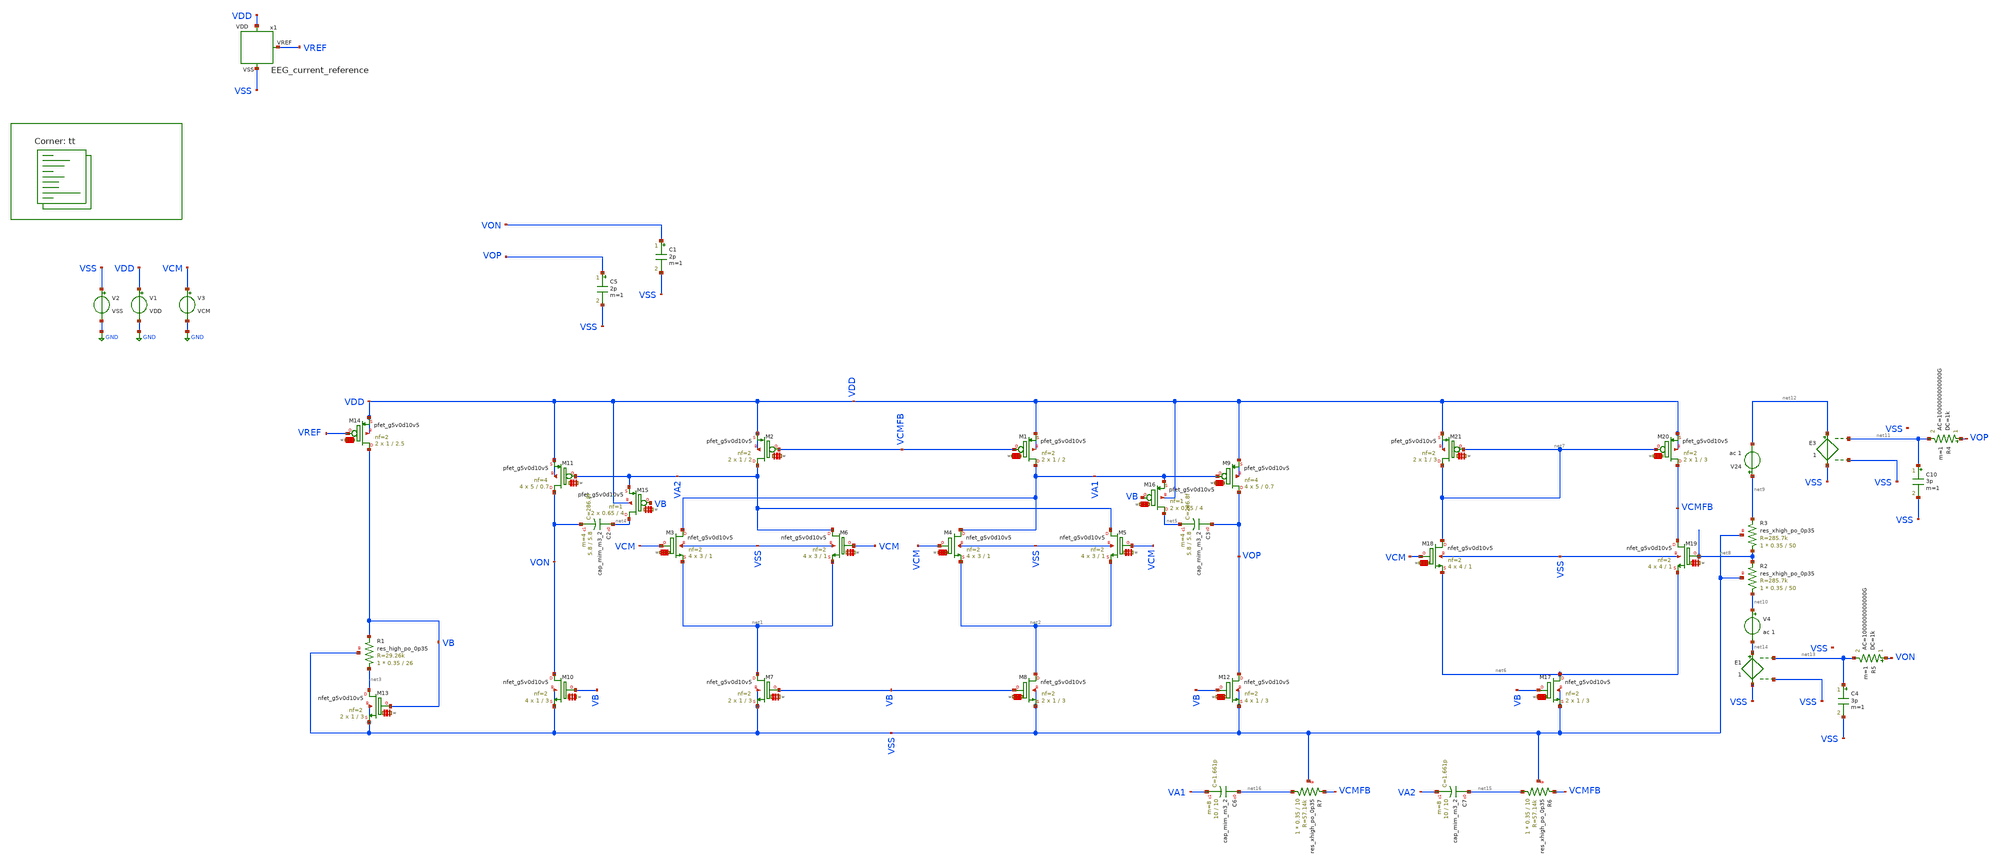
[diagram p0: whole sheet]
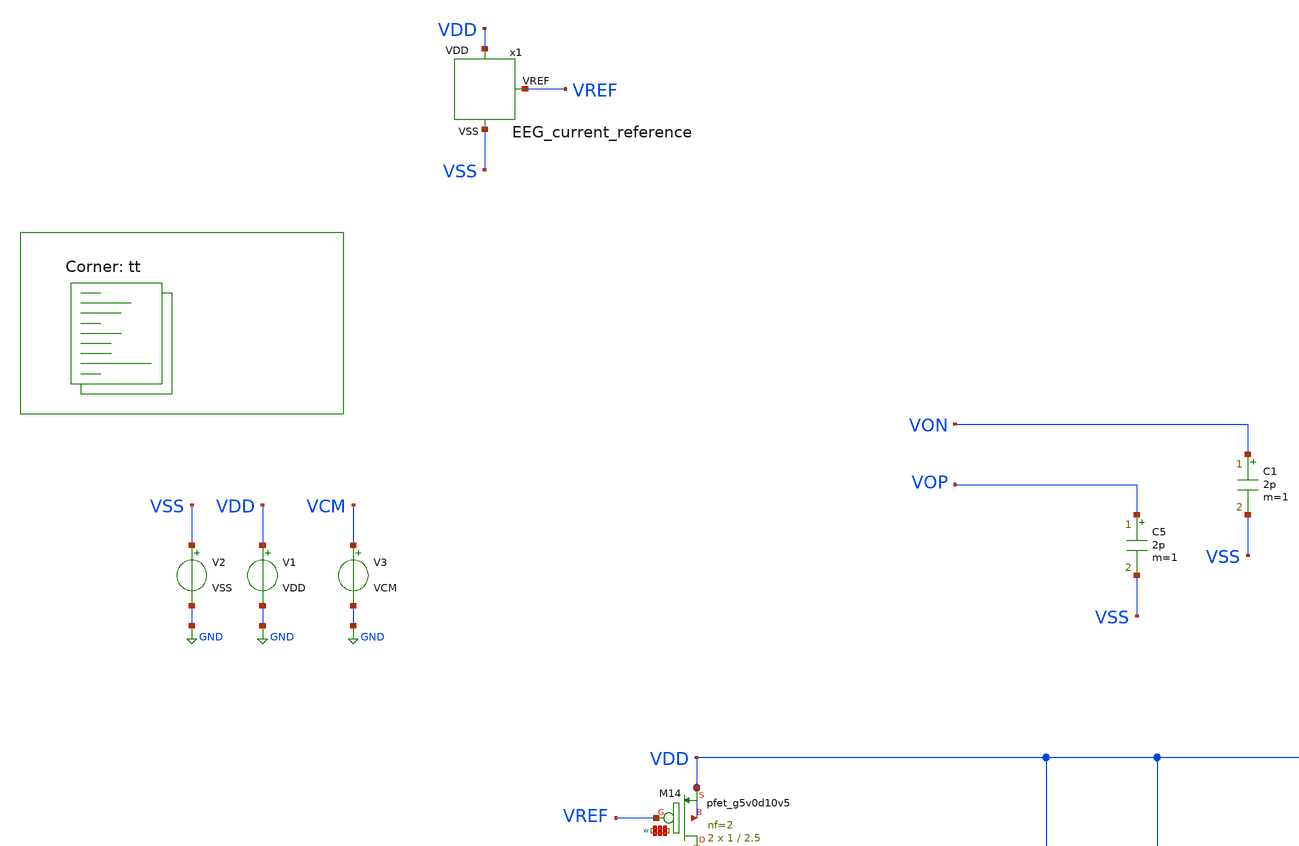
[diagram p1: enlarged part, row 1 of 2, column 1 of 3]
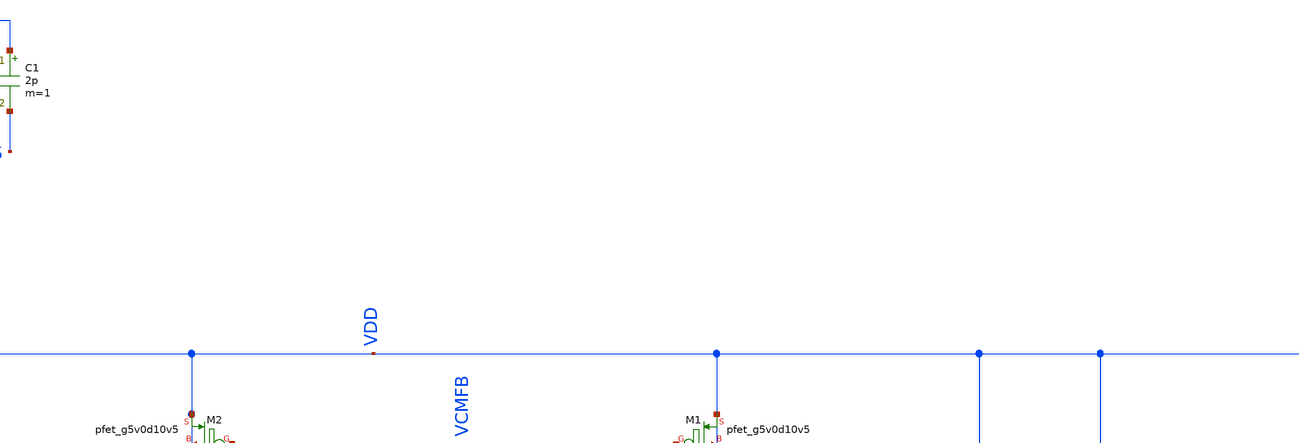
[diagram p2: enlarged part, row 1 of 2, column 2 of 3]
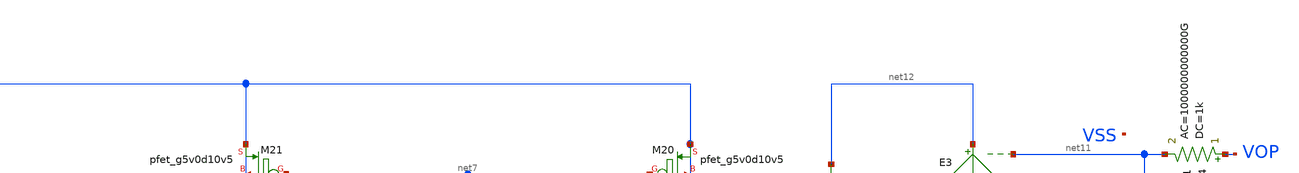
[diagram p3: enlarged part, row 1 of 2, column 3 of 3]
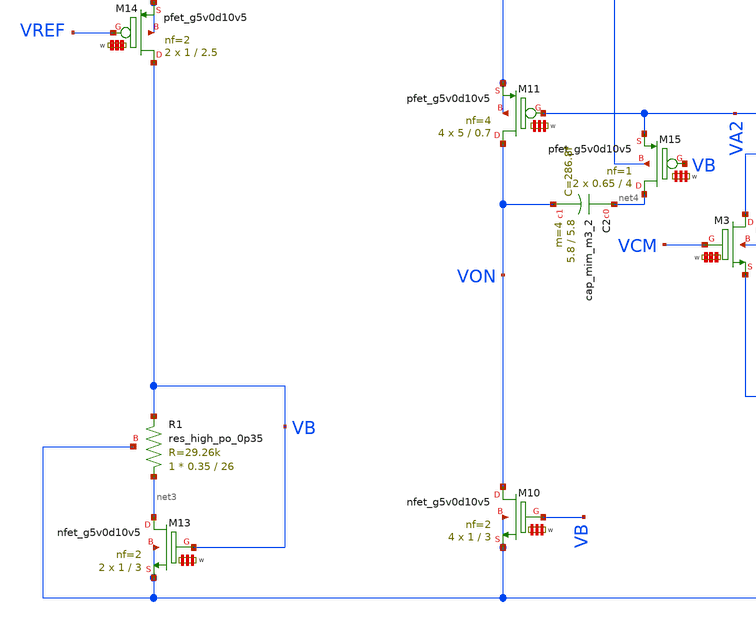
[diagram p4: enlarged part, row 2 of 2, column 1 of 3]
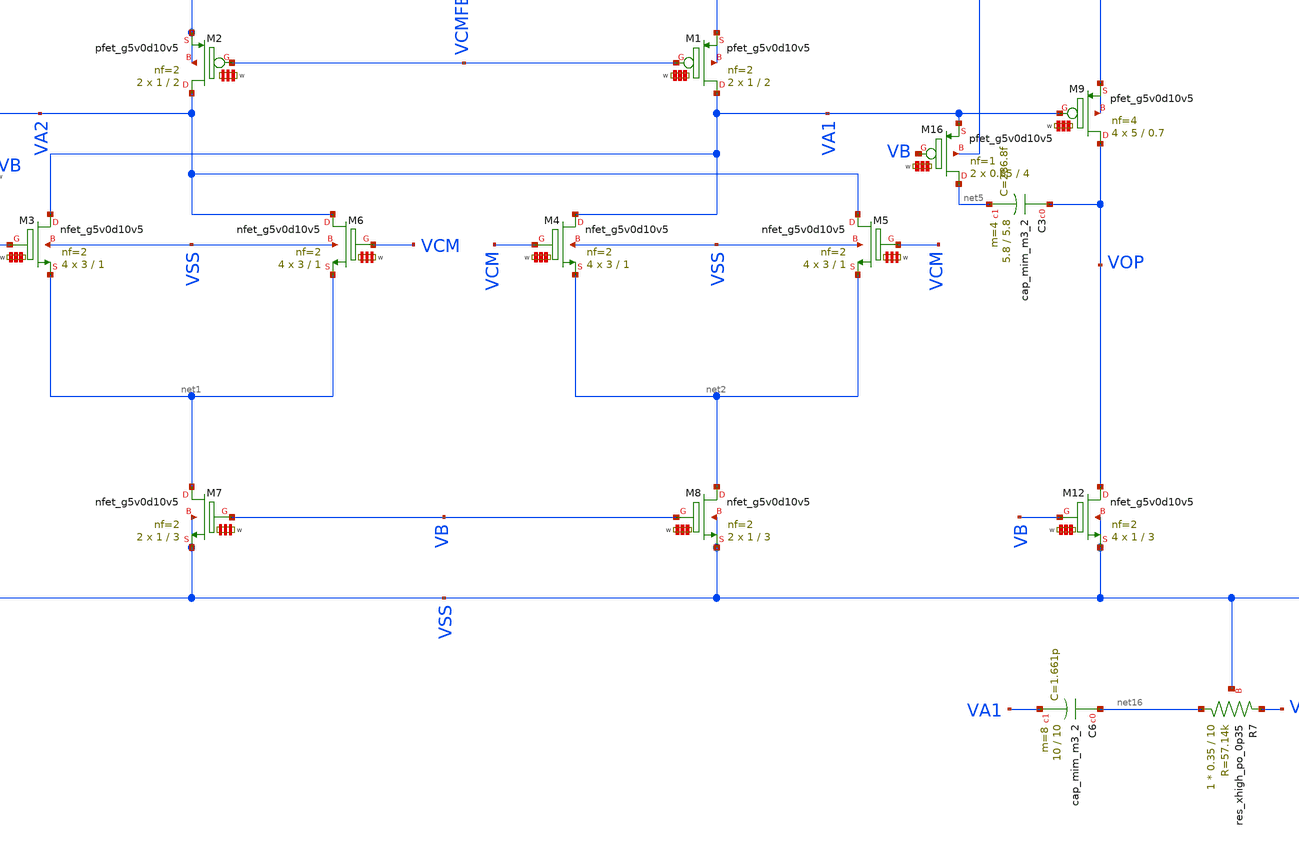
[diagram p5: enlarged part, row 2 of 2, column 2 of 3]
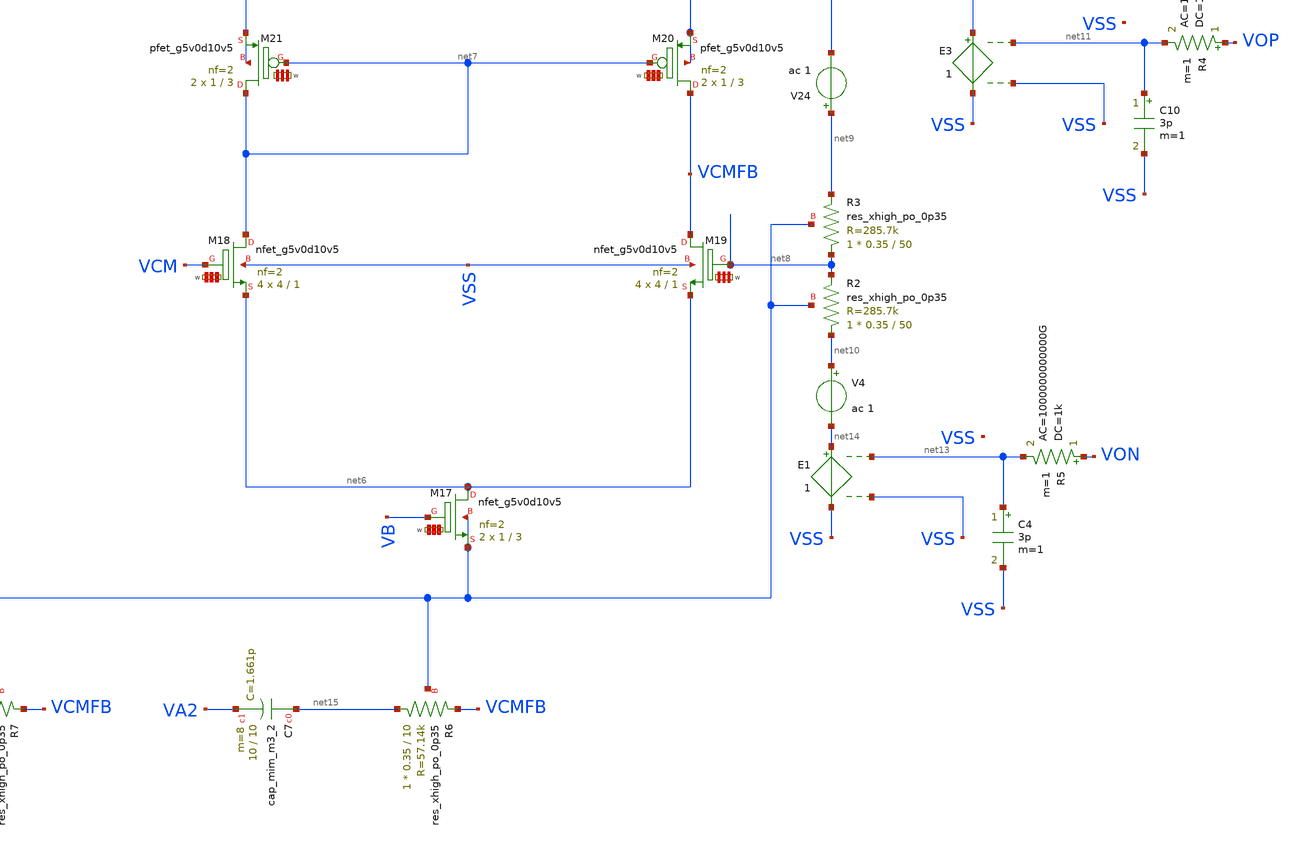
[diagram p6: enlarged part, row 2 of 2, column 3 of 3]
** sch_path: Learning/complex_projects/A_Two-Stage_Time_Division_Multiplexing_AFE_with_Input_Impedance_Boosting_DDA_for_EEG_Signal_Acquisition/sky130A_5V/input_buffer_chopper/stability_cm_tb.sch
**.subckt stability_cm_tb
V1 VDD GND VDD
V2 VSS GND VSS
x1 VDD VSS VREF EEG_current_reference
V3 VCM GND VCM
C5 VOP VSS 2p m=1
C1 VON VSS 2p m=1
XM2 VA2 VCMFB VDD VDD sky130_fd_pr__pfet_g5v0d10v5 L=2 W='1 * 2 ' nf=2 ad='int((2 + 1)/2) * 1 * 0.29'
+ as='int((2 + 2)/2) * 1 * 0.29' pd='2*int((2 + 1)/2) * (1 + 0.29)' ps='2*int((2 + 2)/2) * (1 + 0.29)'
+ nrd='0.29 / 1 / 2 ' nrs='0.29 / 1 / 2 ' sa=0 sb=0 sd=0 mult=2 m=2
XM3 VA1 VCM net1 VSS sky130_fd_pr__nfet_g5v0d10v5 L=1 W='3 * 2 ' nf=2 ad='int((nf+1)/2) * W / nf * 0.29'
+ as='int((nf+2)/2) * W / nf * 0.29' pd='2*int((nf+1)/2) * (W / nf + 0.29)' ps='2*int((nf+2)/2) * (W / nf + 0.29)'
+ nrd='0.29 / W ' nrs='0.29 / W ' sa=0 sb=0 sd=0 mult=4 m=4
XM13 net3 VB VSS VSS sky130_fd_pr__nfet_g5v0d10v5 L=3 W='1 * 2 ' nf=2 ad='int((nf+1)/2) * W / nf * 0.29'
+ as='int((nf+2)/2) * W / nf * 0.29' pd='2*int((nf+1)/2) * (W / nf + 0.29)' ps='2*int((nf+2)/2) * (W / nf + 0.29)'
+ nrd='0.29 / W ' nrs='0.29 / W ' sa=0 sb=0 sd=0 mult=2 m=2
XR1 net3 VB VSS sky130_fd_pr__res_high_po_0p35 L=26 mult=1 m=1
XM14 VB VREF VDD VDD sky130_fd_pr__pfet_g5v0d10v5 L=2.5 W='1 * 2 ' nf=2 ad='int((2 + 1)/2) * 1 * 0.29'
+ as='int((2 + 2)/2) * 1 * 0.29' pd='2*int((2 + 1)/2) * (1 + 0.29)' ps='2*int((2 + 2)/2) * (1 + 0.29)'
+ nrd='0.29 / 1 / 2 ' nrs='0.29 / 1 / 2 ' sa=0 sb=0 sd=0 mult=2 m=2
XM7 net1 VB VSS VSS sky130_fd_pr__nfet_g5v0d10v5 L=3 W='1 * 2 ' nf=2 ad='int((nf+1)/2) * W / nf * 0.29'
+ as='int((nf+2)/2) * W / nf * 0.29' pd='2*int((nf+1)/2) * (W / nf + 0.29)' ps='2*int((nf+2)/2) * (W / nf + 0.29)'
+ nrd='0.29 / W ' nrs='0.29 / W ' sa=0 sb=0 sd=0 mult=2 m=2
XM8 net2 VB VSS VSS sky130_fd_pr__nfet_g5v0d10v5 L=3 W='1 * 2 ' nf=2 ad='int((nf+1)/2) * W / nf * 0.29'
+ as='int((nf+2)/2) * W / nf * 0.29' pd='2*int((nf+1)/2) * (W / nf + 0.29)' ps='2*int((nf+2)/2) * (W / nf + 0.29)'
+ nrd='0.29 / W ' nrs='0.29 / W ' sa=0 sb=0 sd=0 mult=2 m=2
XM10 VON VB VSS VSS sky130_fd_pr__nfet_g5v0d10v5 L=3 W='1 * 2 ' nf=2 ad='int((nf+1)/2) * W / nf * 0.29'
+ as='int((nf+2)/2) * W / nf * 0.29' pd='2*int((nf+1)/2) * (W / nf + 0.29)' ps='2*int((nf+2)/2) * (W / nf + 0.29)'
+ nrd='0.29 / W ' nrs='0.29 / W ' sa=0 sb=0 sd=0 mult=4 m=4
XM12 VOP VB VSS VSS sky130_fd_pr__nfet_g5v0d10v5 L=3 W='1 * 2 ' nf=2 ad='int((nf+1)/2) * W / nf * 0.29'
+ as='int((nf+2)/2) * W / nf * 0.29' pd='2*int((nf+1)/2) * (W / nf + 0.29)' ps='2*int((nf+2)/2) * (W / nf + 0.29)'
+ nrd='0.29 / W ' nrs='0.29 / W ' sa=0 sb=0 sd=0 mult=4 m=4
XM1 VA1 VCMFB VDD VDD sky130_fd_pr__pfet_g5v0d10v5 L=2 W='1 * 2 ' nf=2 ad='int((2 + 1)/2) * 1 * 0.29'
+ as='int((2 + 2)/2) * 1 * 0.29' pd='2*int((2 + 1)/2) * (1 + 0.29)' ps='2*int((2 + 2)/2) * (1 + 0.29)'
+ nrd='0.29 / 1 / 2 ' nrs='0.29 / 1 / 2 ' sa=0 sb=0 sd=0 mult=2 m=2
XM6 VA2 VCM net1 VSS sky130_fd_pr__nfet_g5v0d10v5 L=1 W='3 * 2 ' nf=2 ad='int((nf+1)/2) * W / nf * 0.29'
+ as='int((nf+2)/2) * W / nf * 0.29' pd='2*int((nf+1)/2) * (W / nf + 0.29)' ps='2*int((nf+2)/2) * (W / nf + 0.29)'
+ nrd='0.29 / W ' nrs='0.29 / W ' sa=0 sb=0 sd=0 mult=4 m=4
XM5 VA2 VCM net2 VSS sky130_fd_pr__nfet_g5v0d10v5 L=1 W='3 * 2 ' nf=2 ad='int((nf+1)/2) * W / nf * 0.29'
+ as='int((nf+2)/2) * W / nf * 0.29' pd='2*int((nf+1)/2) * (W / nf + 0.29)' ps='2*int((nf+2)/2) * (W / nf + 0.29)'
+ nrd='0.29 / W ' nrs='0.29 / W ' sa=0 sb=0 sd=0 mult=4 m=4
XM4 VA1 VCM net2 VSS sky130_fd_pr__nfet_g5v0d10v5 L=1 W='3 * 2 ' nf=2 ad='int((nf+1)/2) * W / nf * 0.29'
+ as='int((nf+2)/2) * W / nf * 0.29' pd='2*int((nf+1)/2) * (W / nf + 0.29)' ps='2*int((nf+2)/2) * (W / nf + 0.29)'
+ nrd='0.29 / W ' nrs='0.29 / W ' sa=0 sb=0 sd=0 mult=4 m=4
XM9 VOP VA1 VDD VDD sky130_fd_pr__pfet_g5v0d10v5 L=0.7 W='5 * 4 ' nf=4 ad='int((4 + 1)/2) * 5 * 0.29'
+ as='int((4 + 2)/2) * 5 * 0.29' pd='2*int((4 + 1)/2) * (5 + 0.29)' ps='2*int((4 + 2)/2) * (5 + 0.29)'
+ nrd='0.29 / 5 / 4 ' nrs='0.29 / 5 / 4 ' sa=0 sb=0 sd=0 mult=4 m=4
XM11 VON VA2 VDD VDD sky130_fd_pr__pfet_g5v0d10v5 L=0.7 W='5 * 4 ' nf=4 ad='int((4 + 1)/2) * 5 * 0.29'
+ as='int((4 + 2)/2) * 5 * 0.29' pd='2*int((4 + 1)/2) * (5 + 0.29)' ps='2*int((4 + 2)/2) * (5 + 0.29)'
+ nrd='0.29 / 5 / 4 ' nrs='0.29 / 5 / 4 ' sa=0 sb=0 sd=0 mult=4 m=4
XM17 net6 VB VSS VSS sky130_fd_pr__nfet_g5v0d10v5 L=3 W='1 * 2 ' nf=2 ad='int((nf+1)/2) * W / nf * 0.29'
+ as='int((nf+2)/2) * W / nf * 0.29' pd='2*int((nf+1)/2) * (W / nf + 0.29)' ps='2*int((nf+2)/2) * (W / nf + 0.29)'
+ nrd='0.29 / W ' nrs='0.29 / W ' sa=0 sb=0 sd=0 mult=2 m=2
XM18 net7 VCM net6 VSS sky130_fd_pr__nfet_g5v0d10v5 L=1 W='4 * 2 ' nf=2 ad='int((nf+1)/2) * W / nf * 0.29'
+ as='int((nf+2)/2) * W / nf * 0.29' pd='2*int((nf+1)/2) * (W / nf + 0.29)' ps='2*int((nf+2)/2) * (W / nf + 0.29)'
+ nrd='0.29 / W ' nrs='0.29 / W ' sa=0 sb=0 sd=0 mult=4 m=4
XM19 VCMFB net8 net6 VSS sky130_fd_pr__nfet_g5v0d10v5 L=1 W='4 * 2 ' nf=2 ad='int((nf+1)/2) * W / nf * 0.29'
+ as='int((nf+2)/2) * W / nf * 0.29' pd='2*int((nf+1)/2) * (W / nf + 0.29)' ps='2*int((nf+2)/2) * (W / nf + 0.29)'
+ nrd='0.29 / W ' nrs='0.29 / W ' sa=0 sb=0 sd=0 mult=4 m=4
XM21 net7 net7 VDD VDD sky130_fd_pr__pfet_g5v0d10v5 L=3 W='1 * 2 ' nf=2 ad='int((2 + 1)/2) * 1 * 0.29'
+ as='int((2 + 2)/2) * 1 * 0.29' pd='2*int((2 + 1)/2) * (1 + 0.29)' ps='2*int((2 + 2)/2) * (1 + 0.29)'
+ nrd='0.29 / 1 / 2 ' nrs='0.29 / 1 / 2 ' sa=0 sb=0 sd=0 mult=2 m=2
XM20 VCMFB net7 VDD VDD sky130_fd_pr__pfet_g5v0d10v5 L=3 W='1 * 2 ' nf=2 ad='int((2 + 1)/2) * 1 * 0.29'
+ as='int((2 + 2)/2) * 1 * 0.29' pd='2*int((2 + 1)/2) * (1 + 0.29)' ps='2*int((2 + 2)/2) * (1 + 0.29)'
+ nrd='0.29 / 1 / 2 ' nrs='0.29 / 1 / 2 ' sa=0 sb=0 sd=0 mult=2 m=2
XR3 net8 net9 VSS sky130_fd_pr__res_xhigh_po_0p35 L=50 mult=1 m=1
XR2 net10 net8 VSS sky130_fd_pr__res_xhigh_po_0p35 L=50 mult=1 m=1
E3 net12 VSS net11 VSS 1
R4 VOP net11 1k ac=1000000000000G m=1
C10 net11 VSS 3p m=1
V24 net9 net12 ac 1
E1 net14 VSS net13 VSS 1
R5 VON net13 1k ac=1000000000000G m=1
C4 net13 VSS 3p m=1
V4 net10 net14 ac 1
XC6 net16 VA1 sky130_fd_pr__cap_mim_m3_2 W=10 L=10 MF=8 m=8
XR7 net16 VCMFB VSS sky130_fd_pr__res_xhigh_po_0p35 L=10 mult=1 m=1
XC7 net15 VA2 sky130_fd_pr__cap_mim_m3_2 W=10 L=10 MF=8 m=8
XR6 net15 VCMFB VSS sky130_fd_pr__res_xhigh_po_0p35 L=10 mult=1 m=1
XM15 net4 VB VA2 VDD sky130_fd_pr__pfet_g5v0d10v5 L=4 W='0.65 * 1 ' nf=1 ad='int((1 + 1)/2) * 0.65 * 0.29'
+ as='int((1 + 2)/2) * 0.65 * 0.29' pd='2*int((1 + 1)/2) * (0.65 + 0.29)' ps='2*int((1 + 2)/2) * (0.65 + 0.29)'
+ nrd='0.29 / 0.65 / 1 ' nrs='0.29 / 0.65 / 1 ' sa=0 sb=0 sd=0 mult=2 m=2
XC2 net4 VON sky130_fd_pr__cap_mim_m3_2 W=5.8 L=5.8 MF=4 m=4
XC3 VOP net5 sky130_fd_pr__cap_mim_m3_2 W=5.8 L=5.8 MF=4 m=4
XM16 net5 VB VA1 VDD sky130_fd_pr__pfet_g5v0d10v5 L=4 W='0.65 * 1 ' nf=1 ad='int((1 + 1)/2) * 0.65 * 0.29'
+ as='int((1 + 2)/2) * 0.65 * 0.29' pd='2*int((1 + 1)/2) * (0.65 + 0.29)' ps='2*int((1 + 2)/2) * (0.65 + 0.29)'
+ nrd='0.29 / 0.65 / 1 ' nrs='0.29 / 0.65 / 1 ' sa=0 sb=0 sd=0 mult=2 m=2
**** begin user architecture code
.lib $::SKYWATER_MODELS/sky130.lib.spice tt

.Temp 27
.param VDD = 5
.param VSS = 0
.param CL = 3p
.param V_OFF = -400u
.param VCM = 2.5


.control

	save all
	ac dec 100 1 10G
	plot db(v(VOP)) ((180*ph(v(VOP))/pi))
	op
	print v(VOP)
	print (5*-I(V1))
	*tran 100p 10u
	*plot v(VOP)

.endc




**** end user architecture code
**.ends
.GLOBAL GND
.end
